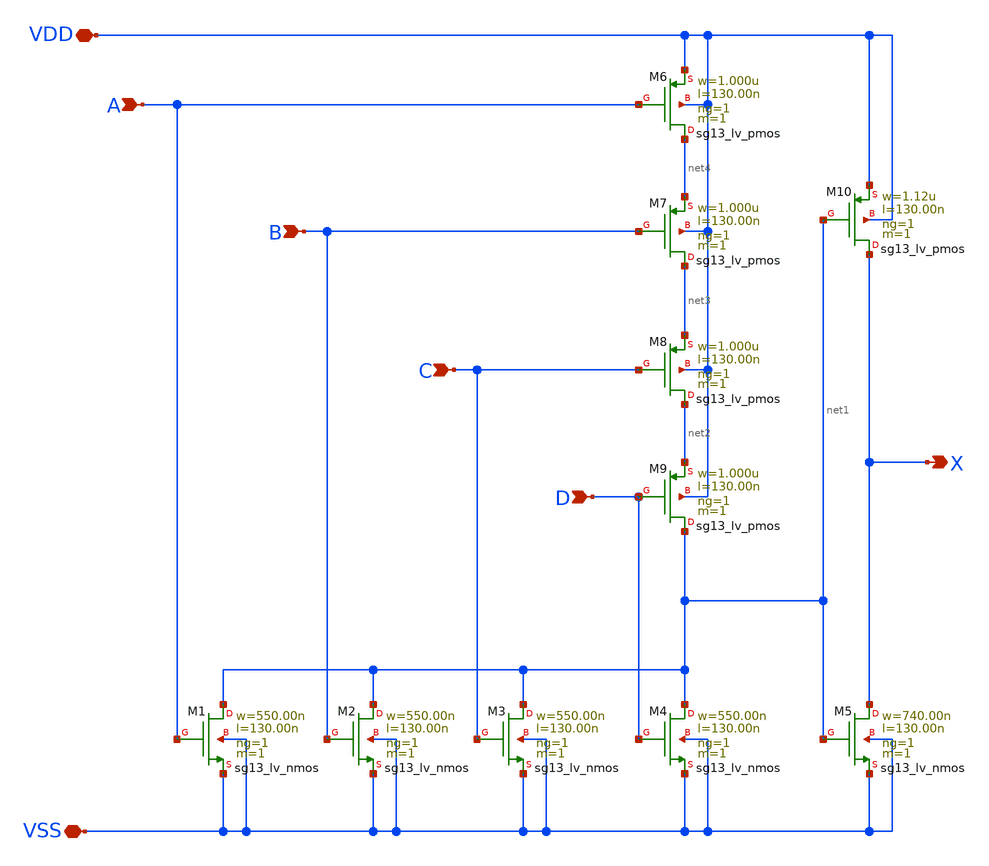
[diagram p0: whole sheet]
** sch_path: ihp-sg13g2/libs.tech/xschem/sg13g2_stdcells/sg13g2_or4_1.sch
* Copyright 2023 IHP PDK Authors
* Licensed under the Apache License, Version 2.0 (the "License");
* you may not use this file except in compliance with the License.
* You may obtain a copy of the License at
* https://www.apache.org/licenses/LICENSE-2.0
* Unless required by applicable law or agreed to in writing, software
* distributed under the License is distributed on an "AS IS" BASIS,
* WITHOUT WARRANTIES OR CONDITIONS OF ANY KIND, either express or implied.
* See the License for the specific language governing permissions and
* limitations under the License.
**.subckt sg13g2_or4_1 X A B C D VDD VSS
*.opin X
*.ipin A
*.ipin B
*.ipin C
*.ipin D
*.iopin VDD
*.iopin VSS
XM1 net1 A VSS VSS sg13_lv_nmos w=550.00n l=130.00n ng=1 m=1 mm_ok=1
XM2 net1 B VSS VSS sg13_lv_nmos w=550.00n l=130.00n ng=1 m=1 mm_ok=1
XM3 net1 C VSS VSS sg13_lv_nmos w=550.00n l=130.00n ng=1 m=1 mm_ok=1
XM4 net1 D VSS VSS sg13_lv_nmos w=550.00n l=130.00n ng=1 m=1 mm_ok=1
XM5 X net1 VSS VSS sg13_lv_nmos w=740.00n l=130.00n ng=1 m=1 mm_ok=1
XM6 net4 A VDD VDD sg13_lv_pmos w=1.000u l=130.00n ng=1 m=1 mm_ok=1
XM7 net3 B net4 VDD sg13_lv_pmos w=1.000u l=130.00n ng=1 m=1 mm_ok=1
XM8 net2 C net3 VDD sg13_lv_pmos w=1.000u l=130.00n ng=1 m=1 mm_ok=1
XM9 net1 D net2 VDD sg13_lv_pmos w=1.000u l=130.00n ng=1 m=1 mm_ok=1
XM10 X net1 VDD VDD sg13_lv_pmos w=1.12u l=130.00n ng=1 m=1 mm_ok=1
**.ends
.end
